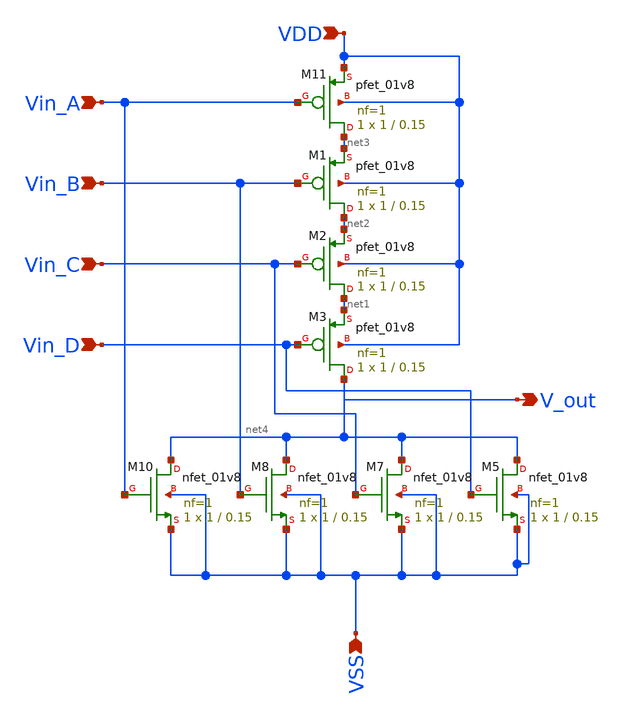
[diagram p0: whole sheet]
** sch_path: schematics_xschem/ORgate.sch
**.subckt ORgate Vin_A Vin_B Vin_C Vin_D V_out VSS VDD
*.ipin Vin_A
*.ipin Vin_B
*.ipin Vin_C
*.ipin Vin_D
*.opin V_out
*.ipin VSS
*.ipin VDD
XM5 net4 Vin_D VSS VSS sky130_fd_pr__nfet_01v8 L=0.15 W=1 nf=1 ad='int((nf+1)/2) * W/nf * 0.29' as='int((nf+2)/2) * W/nf * 0.29'
+ pd='2*int((nf+1)/2) * (W/nf + 0.29)' ps='2*int((nf+2)/2) * (W/nf + 0.29)' nrd='0.29 / W' nrs='0.29 / W'
+ sa=0 sb=0 sd=0 mult=1 m=1
XM7 net4 Vin_C VSS VSS sky130_fd_pr__nfet_01v8 L=0.15 W=1 nf=1 ad='int((nf+1)/2) * W/nf * 0.29' as='int((nf+2)/2) * W/nf * 0.29'
+ pd='2*int((nf+1)/2) * (W/nf + 0.29)' ps='2*int((nf+2)/2) * (W/nf + 0.29)' nrd='0.29 / W' nrs='0.29 / W'
+ sa=0 sb=0 sd=0 mult=1 m=1
XM8 net4 Vin_B VSS VSS sky130_fd_pr__nfet_01v8 L=0.15 W=1 nf=1 ad='int((nf+1)/2) * W/nf * 0.29' as='int((nf+2)/2) * W/nf * 0.29'
+ pd='2*int((nf+1)/2) * (W/nf + 0.29)' ps='2*int((nf+2)/2) * (W/nf + 0.29)' nrd='0.29 / W' nrs='0.29 / W'
+ sa=0 sb=0 sd=0 mult=1 m=1
XM10 net4 Vin_A VSS VSS sky130_fd_pr__nfet_01v8 L=0.15 W=1 nf=1 ad='int((nf+1)/2) * W/nf * 0.29' as='int((nf+2)/2) * W/nf * 0.29'
+ pd='2*int((nf+1)/2) * (W/nf + 0.29)' ps='2*int((nf+2)/2) * (W/nf + 0.29)' nrd='0.29 / W' nrs='0.29 / W'
+ sa=0 sb=0 sd=0 mult=1 m=1
XM11 net3 Vin_A VDD VDD sky130_fd_pr__pfet_01v8 L=0.15 W=1 nf=1 ad='int((nf+1)/2) * W/nf * 0.29' as='int((nf+2)/2) * W/nf * 0.29'
+ pd='2*int((nf+1)/2) * (W/nf + 0.29)' ps='2*int((nf+2)/2) * (W/nf + 0.29)' nrd='0.29 / W' nrs='0.29 / W'
+ sa=0 sb=0 sd=0 mult=1 m=1
XM1 net2 Vin_B net3 VDD sky130_fd_pr__pfet_01v8 L=0.15 W=1 nf=1 ad='int((nf+1)/2) * W/nf * 0.29' as='int((nf+2)/2) * W/nf * 0.29'
+ pd='2*int((nf+1)/2) * (W/nf + 0.29)' ps='2*int((nf+2)/2) * (W/nf + 0.29)' nrd='0.29 / W' nrs='0.29 / W'
+ sa=0 sb=0 sd=0 mult=1 m=1
XM2 net1 Vin_C net2 VDD sky130_fd_pr__pfet_01v8 L=0.15 W=1 nf=1 ad='int((nf+1)/2) * W/nf * 0.29' as='int((nf+2)/2) * W/nf * 0.29'
+ pd='2*int((nf+1)/2) * (W/nf + 0.29)' ps='2*int((nf+2)/2) * (W/nf + 0.29)' nrd='0.29 / W' nrs='0.29 / W'
+ sa=0 sb=0 sd=0 mult=1 m=1
XM3 net4 Vin_D net1 VDD sky130_fd_pr__pfet_01v8 L=0.15 W=1 nf=1 ad='int((nf+1)/2) * W/nf * 0.29' as='int((nf+2)/2) * W/nf * 0.29'
+ pd='2*int((nf+1)/2) * (W/nf + 0.29)' ps='2*int((nf+2)/2) * (W/nf + 0.29)' nrd='0.29 / W' nrs='0.29 / W'
+ sa=0 sb=0 sd=0 mult=1 m=1
**.ends
.end
